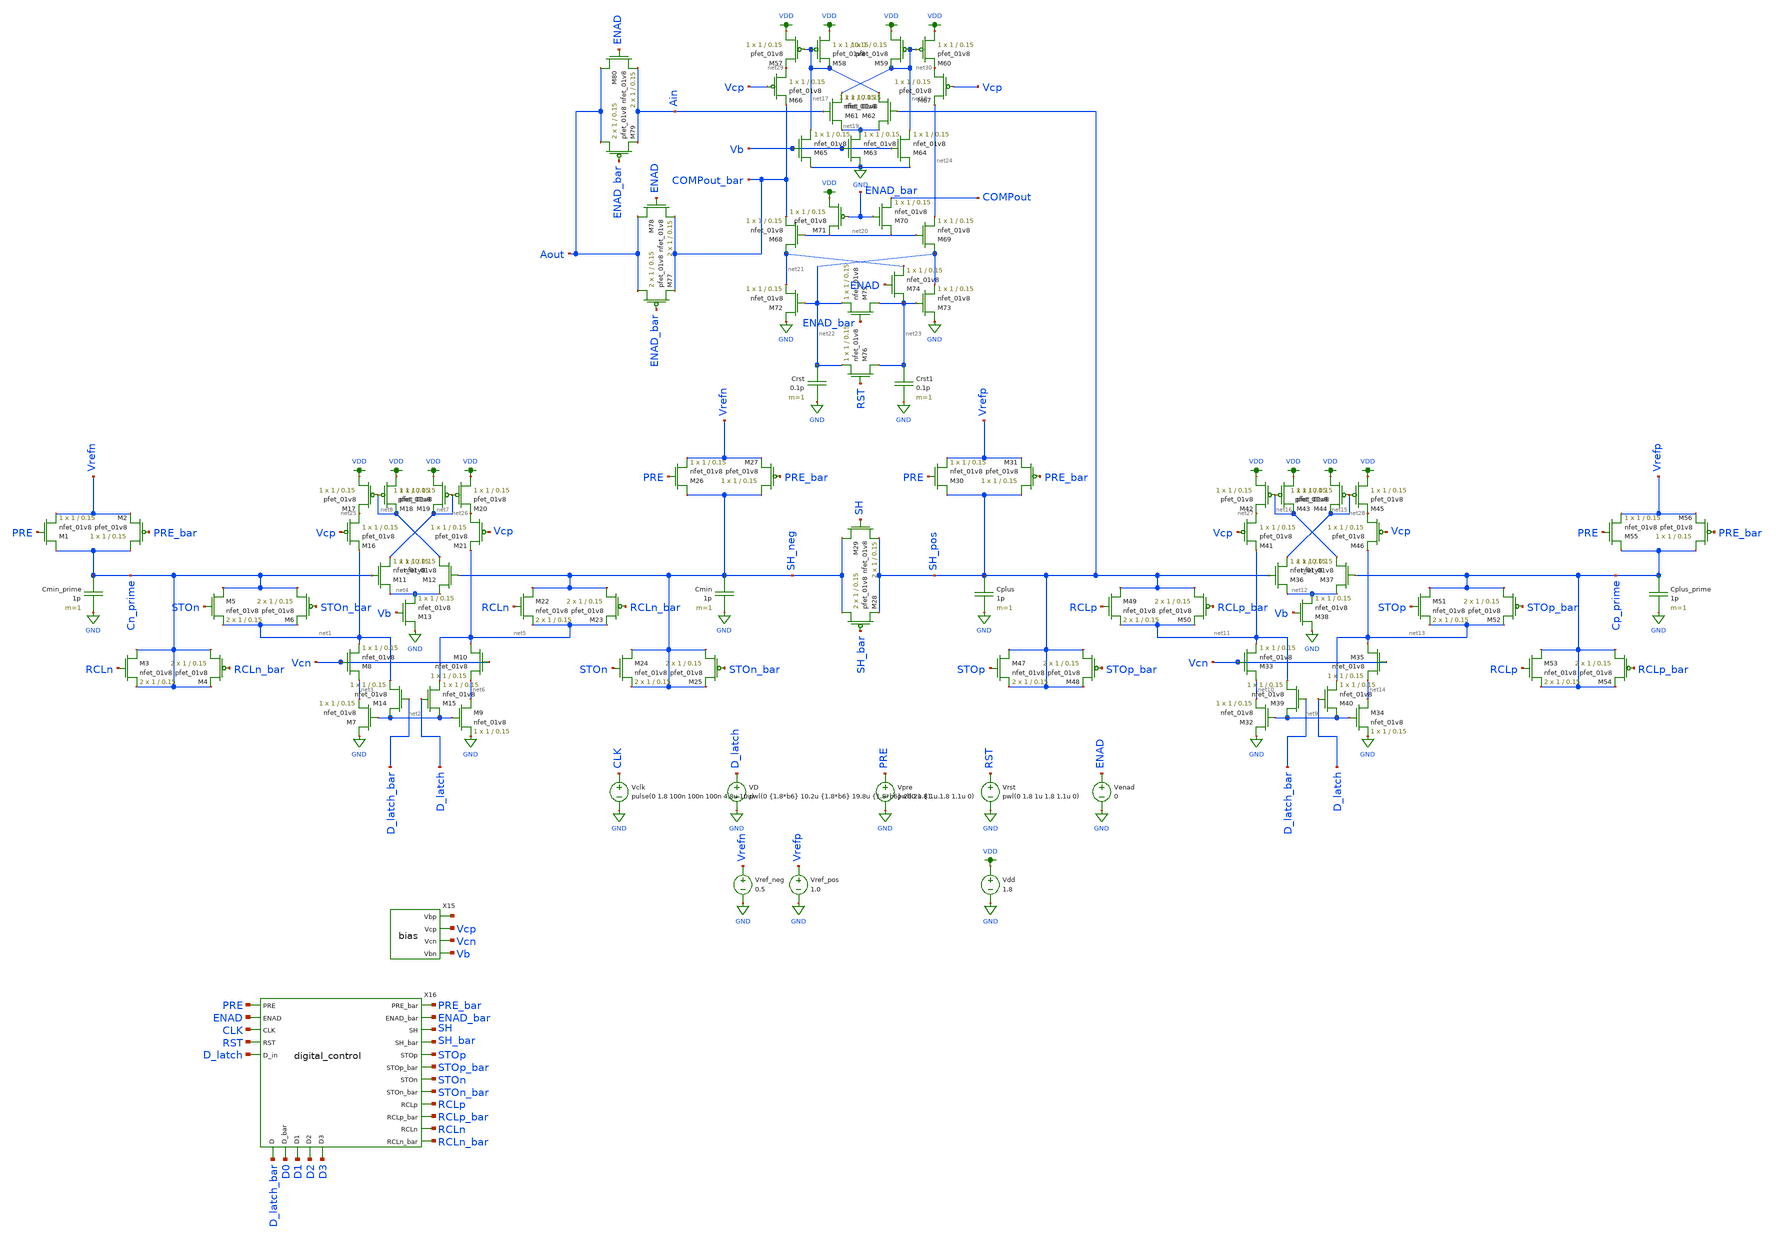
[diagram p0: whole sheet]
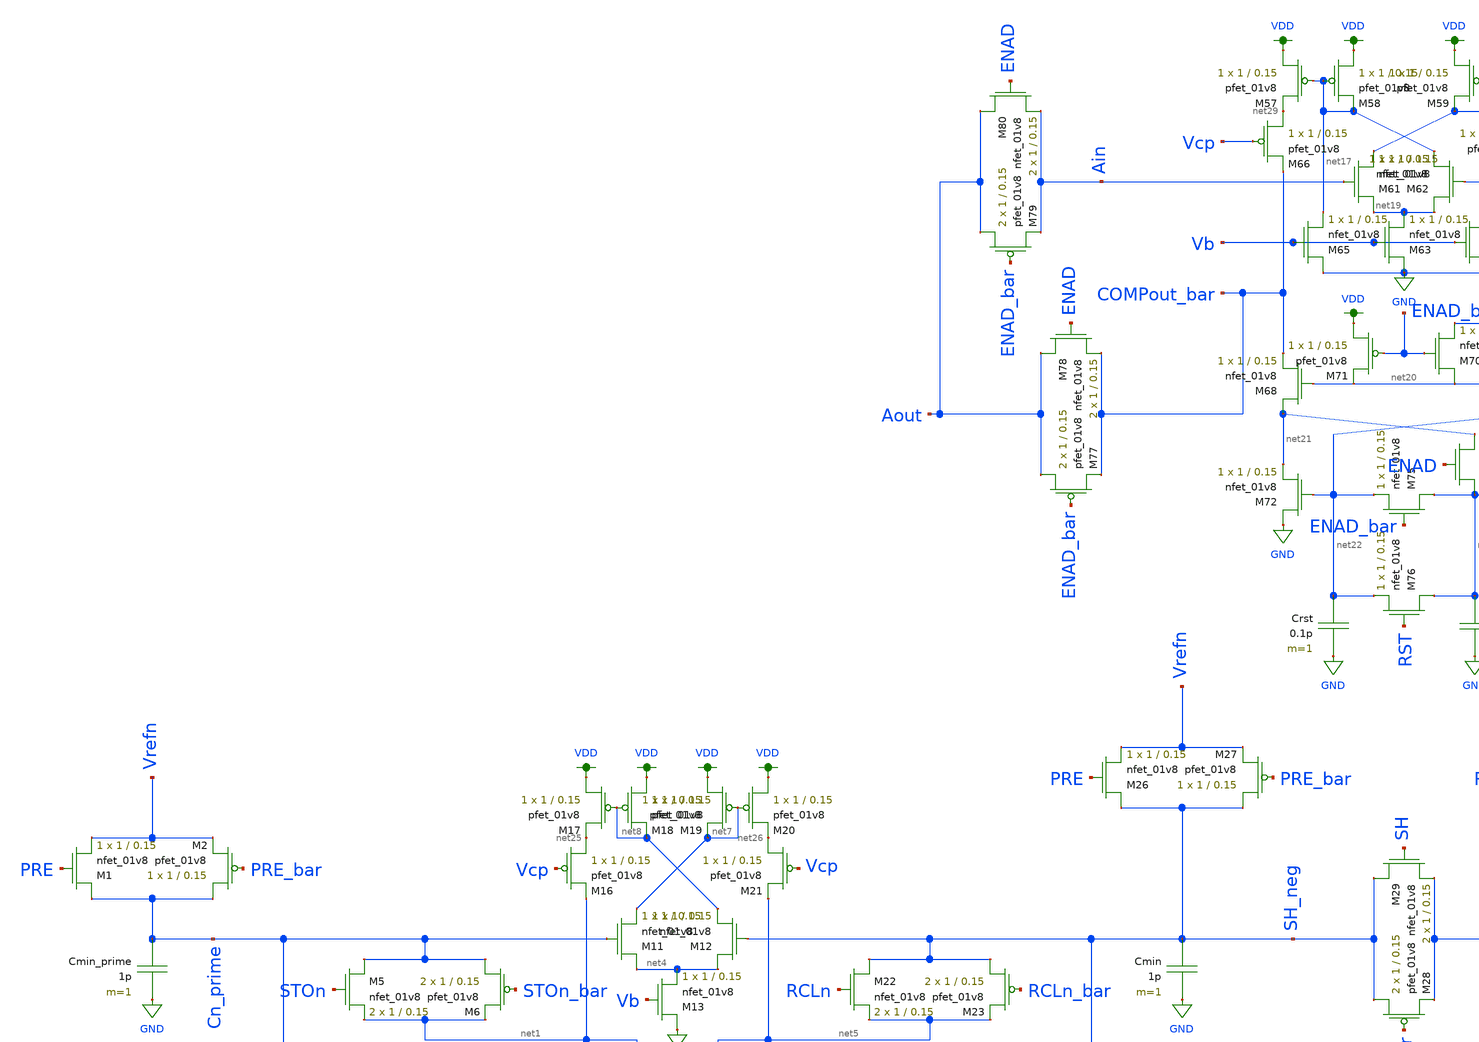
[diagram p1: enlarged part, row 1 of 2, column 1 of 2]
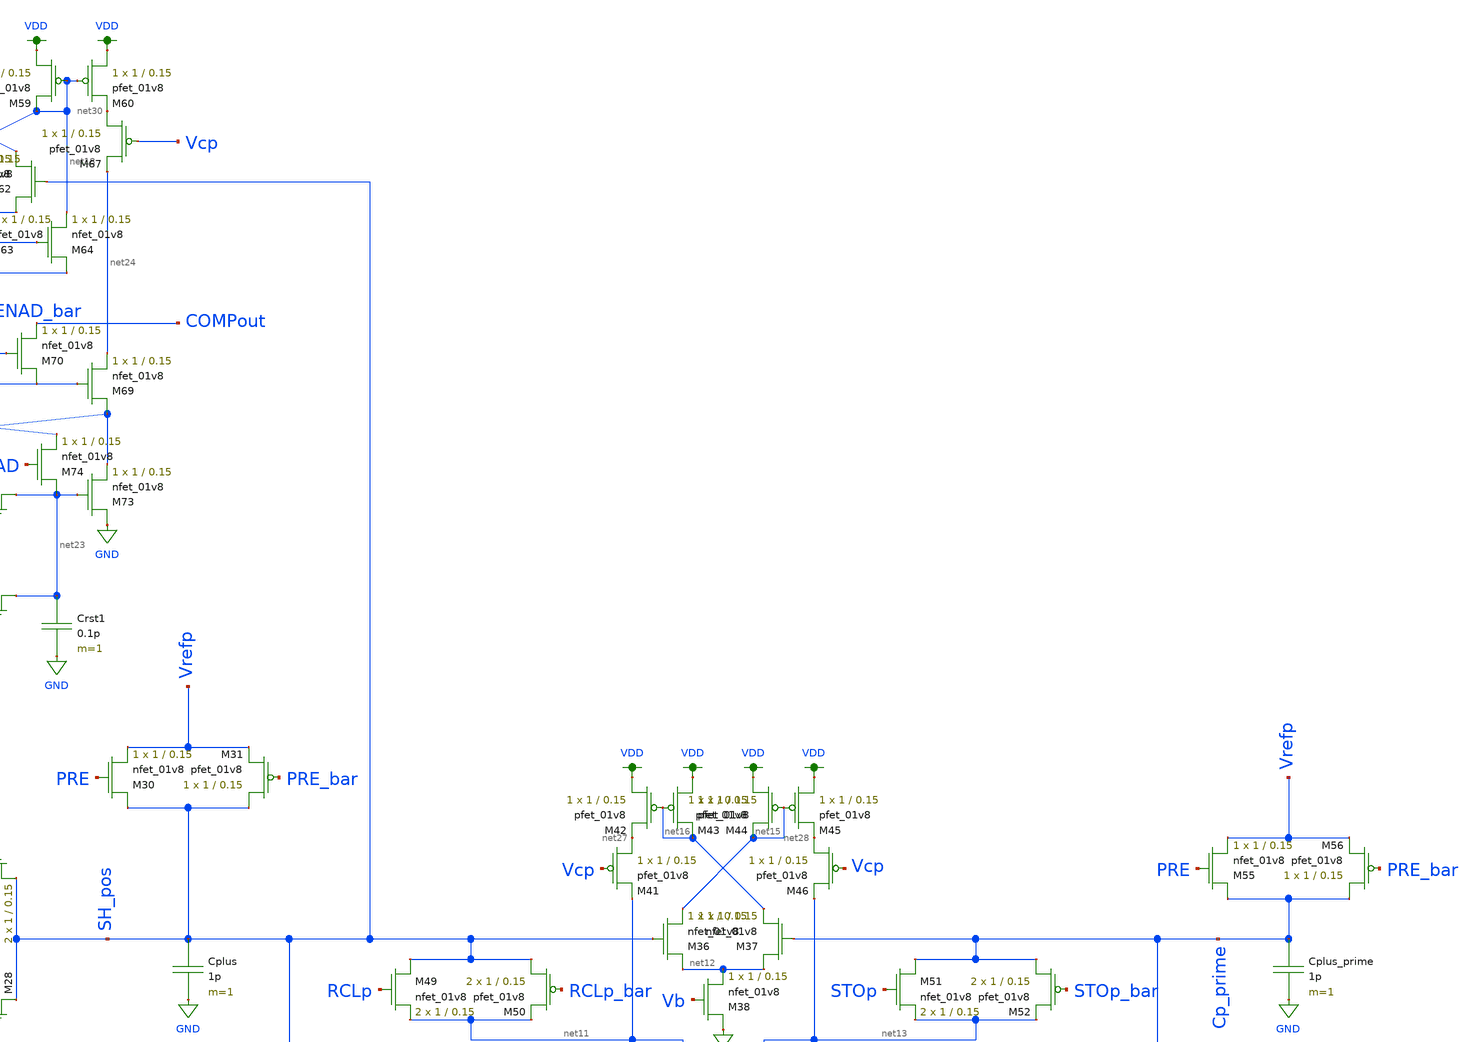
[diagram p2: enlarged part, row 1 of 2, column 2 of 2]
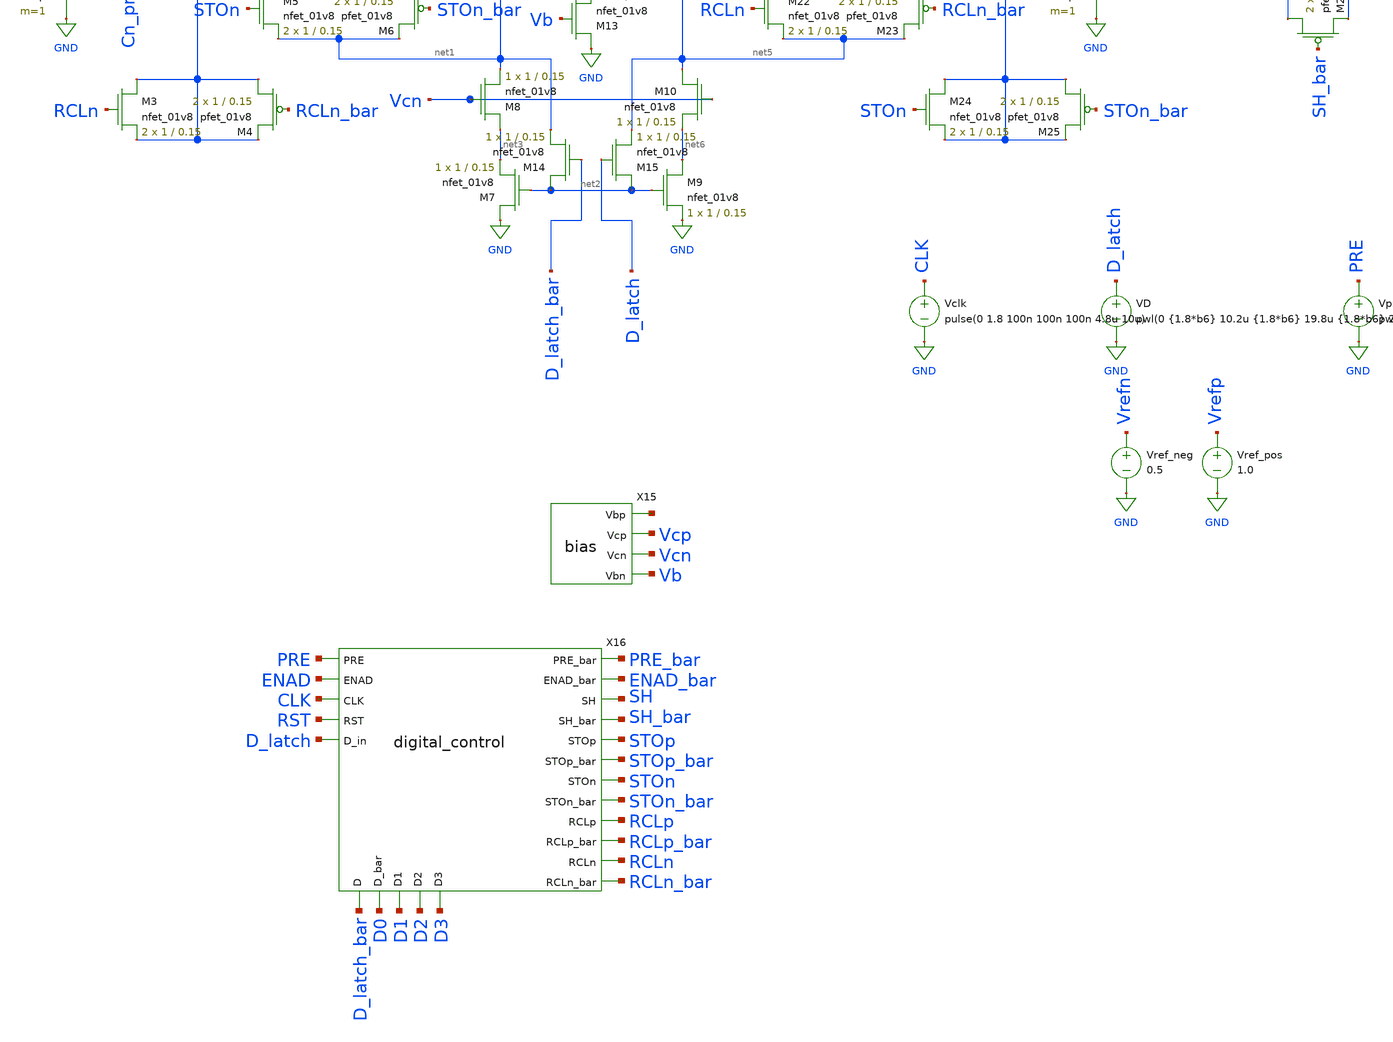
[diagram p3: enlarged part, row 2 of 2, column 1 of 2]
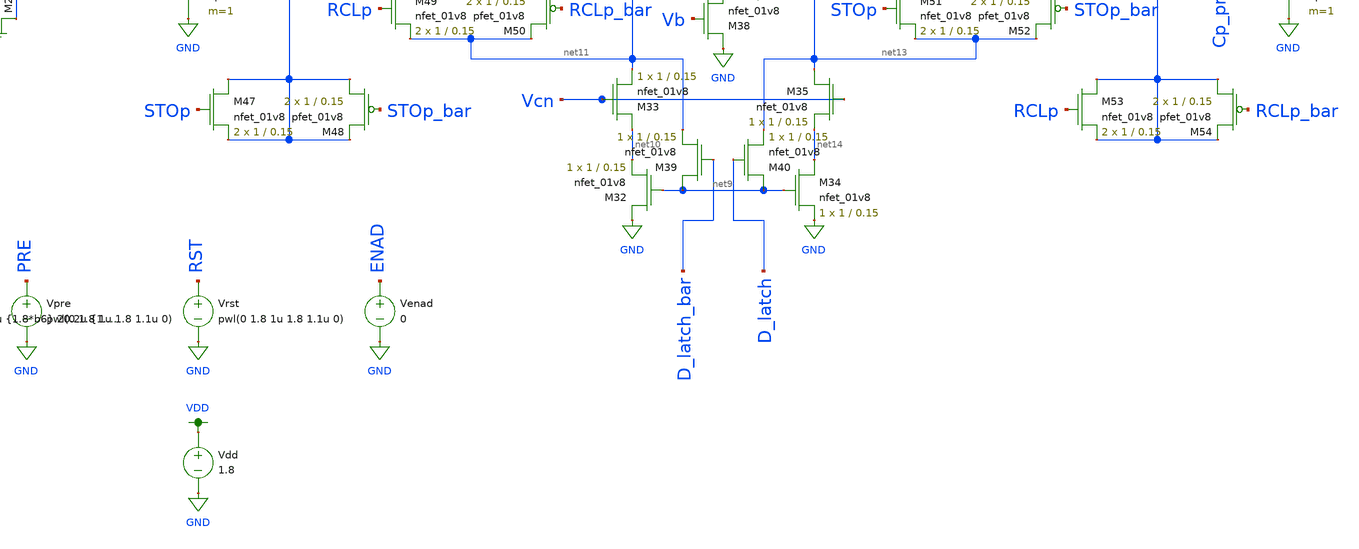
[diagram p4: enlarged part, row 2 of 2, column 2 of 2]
** sch_path: simulations/test_harness_dac_7bit.sch
**.subckt test_harness_dac_7bit
XM1 Cn_prime PRE Vrefn GND sky130_fd_pr__nfet_01v8 L=0.15 W=1 nf=1 ad='int((nf+1)/2) * W/nf * 0.29' as='int((nf+2)/2) * W/nf * 0.29'
+ pd='2*int((nf+1)/2) * (W/nf + 0.29)' ps='2*int((nf+2)/2) * (W/nf + 0.29)' nrd='0.29 / W' nrs='0.29 / W'
+ sa=0 sb=0 sd=0 mult=1 m=1
XM2 Cn_prime PRE_bar Vrefn VDD sky130_fd_pr__pfet_01v8 L=0.15 W=1 nf=1 ad='int((nf+1)/2) * W/nf * 0.29'
+ as='int((nf+2)/2) * W/nf * 0.29' pd='2*int((nf+1)/2) * (W/nf + 0.29)' ps='2*int((nf+2)/2) * (W/nf + 0.29)'
+ nrd='0.29 / W' nrs='0.29 / W' sa=0 sb=0 sd=0 mult=1 m=1
Cmin_prime Cn_prime GND 1p m=1
XM3 Cn_prime RCLn Cn_prime GND sky130_fd_pr__nfet_01v8 L=0.15 W=1 nf=1 ad='int((nf+1)/2) * W/nf * 0.29'
+ as='int((nf+2)/2) * W/nf * 0.29' pd='2*int((nf+1)/2) * (W/nf + 0.29)' ps='2*int((nf+2)/2) * (W/nf + 0.29)'
+ nrd='0.29 / W' nrs='0.29 / W' sa=0 sb=0 sd=0 mult=2 m=2
XM4 Cn_prime RCLn_bar Cn_prime VDD sky130_fd_pr__pfet_01v8 L=0.15 W=1 nf=1 ad='int((nf+1)/2) * W/nf * 0.29'
+ as='int((nf+2)/2) * W/nf * 0.29' pd='2*int((nf+1)/2) * (W/nf + 0.29)' ps='2*int((nf+2)/2) * (W/nf + 0.29)'
+ nrd='0.29 / W' nrs='0.29 / W' sa=0 sb=0 sd=0 mult=2 m=2
XM5 Cn_prime STOn net1 GND sky130_fd_pr__nfet_01v8 L=0.15 W=1 nf=1 ad='int((nf+1)/2) * W/nf * 0.29' as='int((nf+2)/2) * W/nf * 0.29'
+ pd='2*int((nf+1)/2) * (W/nf + 0.29)' ps='2*int((nf+2)/2) * (W/nf + 0.29)' nrd='0.29 / W' nrs='0.29 / W'
+ sa=0 sb=0 sd=0 mult=2 m=2
XM6 Cn_prime STOn_bar net1 VDD sky130_fd_pr__pfet_01v8 L=0.15 W=1 nf=1 ad='int((nf+1)/2) * W/nf * 0.29'
+ as='int((nf+2)/2) * W/nf * 0.29' pd='2*int((nf+1)/2) * (W/nf + 0.29)' ps='2*int((nf+2)/2) * (W/nf + 0.29)'
+ nrd='0.29 / W' nrs='0.29 / W' sa=0 sb=0 sd=0 mult=2 m=2
XM7 GND net2 net3 GND sky130_fd_pr__nfet_01v8 L=0.15 W=1 nf=1 ad='int((nf+1)/2) * W/nf * 0.29' as='int((nf+2)/2) * W/nf * 0.29'
+ pd='2*int((nf+1)/2) * (W/nf + 0.29)' ps='2*int((nf+2)/2) * (W/nf + 0.29)' nrd='0.29 / W' nrs='0.29 / W'
+ sa=0 sb=0 sd=0 mult=1 m=1
XM8 net3 Vcn net1 GND sky130_fd_pr__nfet_01v8 L=0.15 W=1 nf=1 ad='int((nf+1)/2) * W/nf * 0.29' as='int((nf+2)/2) * W/nf * 0.29'
+ pd='2*int((nf+1)/2) * (W/nf + 0.29)' ps='2*int((nf+2)/2) * (W/nf + 0.29)' nrd='0.29 / W' nrs='0.29 / W'
+ sa=0 sb=0 sd=0 mult=1 m=1
XM9 net6 net2 GND GND sky130_fd_pr__nfet_01v8 L=0.15 W=1 nf=1 ad='int((nf+1)/2) * W/nf * 0.29' as='int((nf+2)/2) * W/nf * 0.29'
+ pd='2*int((nf+1)/2) * (W/nf + 0.29)' ps='2*int((nf+2)/2) * (W/nf + 0.29)' nrd='0.29 / W' nrs='0.29 / W'
+ sa=0 sb=0 sd=0 mult=1 m=1
XM10 net5 Vcn net6 GND sky130_fd_pr__nfet_01v8 L=0.15 W=1 nf=1 ad='int((nf+1)/2) * W/nf * 0.29' as='int((nf+2)/2) * W/nf * 0.29'
+ pd='2*int((nf+1)/2) * (W/nf + 0.29)' ps='2*int((nf+2)/2) * (W/nf + 0.29)' nrd='0.29 / W' nrs='0.29 / W'
+ sa=0 sb=0 sd=0 mult=1 m=1
XM11 net4 Cn_prime net7 GND sky130_fd_pr__nfet_01v8 L=0.15 W=1 nf=1 ad='int((nf+1)/2) * W/nf * 0.29'
+ as='int((nf+2)/2) * W/nf * 0.29' pd='2*int((nf+1)/2) * (W/nf + 0.29)' ps='2*int((nf+2)/2) * (W/nf + 0.29)'
+ nrd='0.29 / W' nrs='0.29 / W' sa=0 sb=0 sd=0 mult=1 m=1
XM12 net4 SH_neg net8 GND sky130_fd_pr__nfet_01v8 L=0.15 W=1 nf=1 ad='int((nf+1)/2) * W/nf * 0.29' as='int((nf+2)/2) * W/nf * 0.29'
+ pd='2*int((nf+1)/2) * (W/nf + 0.29)' ps='2*int((nf+2)/2) * (W/nf + 0.29)' nrd='0.29 / W' nrs='0.29 / W'
+ sa=0 sb=0 sd=0 mult=1 m=1
XM13 GND Vb net4 GND sky130_fd_pr__nfet_01v8 L=0.15 W=1 nf=1 ad='int((nf+1)/2) * W/nf * 0.29' as='int((nf+2)/2) * W/nf * 0.29'
+ pd='2*int((nf+1)/2) * (W/nf + 0.29)' ps='2*int((nf+2)/2) * (W/nf + 0.29)' nrd='0.29 / W' nrs='0.29 / W'
+ sa=0 sb=0 sd=0 mult=1 m=1
XM14 net2 D_latch_bar net1 GND sky130_fd_pr__nfet_01v8 L=0.15 W=1 nf=1 ad='int((nf+1)/2) * W/nf * 0.29'
+ as='int((nf+2)/2) * W/nf * 0.29' pd='2*int((nf+1)/2) * (W/nf + 0.29)' ps='2*int((nf+2)/2) * (W/nf + 0.29)'
+ nrd='0.29 / W' nrs='0.29 / W' sa=0 sb=0 sd=0 mult=1 m=1
XM15 net2 D_latch net5 GND sky130_fd_pr__nfet_01v8 L=0.15 W=1 nf=1 ad='int((nf+1)/2) * W/nf * 0.29' as='int((nf+2)/2) * W/nf * 0.29'
+ pd='2*int((nf+1)/2) * (W/nf + 0.29)' ps='2*int((nf+2)/2) * (W/nf + 0.29)' nrd='0.29 / W' nrs='0.29 / W'
+ sa=0 sb=0 sd=0 mult=1 m=1
XM16 net25 Vcp net1 VDD sky130_fd_pr__pfet_01v8 L=0.15 W=1 nf=1 ad='int((nf+1)/2) * W/nf * 0.29' as='int((nf+2)/2) * W/nf * 0.29'
+ pd='2*int((nf+1)/2) * (W/nf + 0.29)' ps='2*int((nf+2)/2) * (W/nf + 0.29)' nrd='0.29 / W' nrs='0.29 / W'
+ sa=0 sb=0 sd=0 mult=1 m=1
XM17 VDD net8 net25 VDD sky130_fd_pr__pfet_01v8 L=0.15 W=1 nf=1 ad='int((nf+1)/2) * W/nf * 0.29' as='int((nf+2)/2) * W/nf * 0.29'
+ pd='2*int((nf+1)/2) * (W/nf + 0.29)' ps='2*int((nf+2)/2) * (W/nf + 0.29)' nrd='0.29 / W' nrs='0.29 / W'
+ sa=0 sb=0 sd=0 mult=1 m=1
XM18 VDD net8 net8 VDD sky130_fd_pr__pfet_01v8 L=0.15 W=1 nf=1 ad='int((nf+1)/2) * W/nf * 0.29' as='int((nf+2)/2) * W/nf * 0.29'
+ pd='2*int((nf+1)/2) * (W/nf + 0.29)' ps='2*int((nf+2)/2) * (W/nf + 0.29)' nrd='0.29 / W' nrs='0.29 / W'
+ sa=0 sb=0 sd=0 mult=1 m=1
XM19 VDD net7 net7 VDD sky130_fd_pr__pfet_01v8 L=0.15 W=1 nf=1 ad='int((nf+1)/2) * W/nf * 0.29' as='int((nf+2)/2) * W/nf * 0.29'
+ pd='2*int((nf+1)/2) * (W/nf + 0.29)' ps='2*int((nf+2)/2) * (W/nf + 0.29)' nrd='0.29 / W' nrs='0.29 / W'
+ sa=0 sb=0 sd=0 mult=1 m=1
XM20 VDD net7 net26 VDD sky130_fd_pr__pfet_01v8 L=0.15 W=1 nf=1 ad='int((nf+1)/2) * W/nf * 0.29' as='int((nf+2)/2) * W/nf * 0.29'
+ pd='2*int((nf+1)/2) * (W/nf + 0.29)' ps='2*int((nf+2)/2) * (W/nf + 0.29)' nrd='0.29 / W' nrs='0.29 / W'
+ sa=0 sb=0 sd=0 mult=1 m=1
XM21 net26 Vcp net5 VDD sky130_fd_pr__pfet_01v8 L=0.15 W=1 nf=1 ad='int((nf+1)/2) * W/nf * 0.29' as='int((nf+2)/2) * W/nf * 0.29'
+ pd='2*int((nf+1)/2) * (W/nf + 0.29)' ps='2*int((nf+2)/2) * (W/nf + 0.29)' nrd='0.29 / W' nrs='0.29 / W'
+ sa=0 sb=0 sd=0 mult=1 m=1
XM22 SH_neg RCLn net5 GND sky130_fd_pr__nfet_01v8 L=0.15 W=1 nf=1 ad='int((nf+1)/2) * W/nf * 0.29' as='int((nf+2)/2) * W/nf * 0.29'
+ pd='2*int((nf+1)/2) * (W/nf + 0.29)' ps='2*int((nf+2)/2) * (W/nf + 0.29)' nrd='0.29 / W' nrs='0.29 / W'
+ sa=0 sb=0 sd=0 mult=2 m=2
XM23 SH_neg RCLn_bar net5 VDD sky130_fd_pr__pfet_01v8 L=0.15 W=1 nf=1 ad='int((nf+1)/2) * W/nf * 0.29'
+ as='int((nf+2)/2) * W/nf * 0.29' pd='2*int((nf+1)/2) * (W/nf + 0.29)' ps='2*int((nf+2)/2) * (W/nf + 0.29)'
+ nrd='0.29 / W' nrs='0.29 / W' sa=0 sb=0 sd=0 mult=2 m=2
XM24 SH_neg STOn SH_neg GND sky130_fd_pr__nfet_01v8 L=0.15 W=1 nf=1 ad='int((nf+1)/2) * W/nf * 0.29'
+ as='int((nf+2)/2) * W/nf * 0.29' pd='2*int((nf+1)/2) * (W/nf + 0.29)' ps='2*int((nf+2)/2) * (W/nf + 0.29)'
+ nrd='0.29 / W' nrs='0.29 / W' sa=0 sb=0 sd=0 mult=2 m=2
XM25 SH_neg STOn_bar SH_neg VDD sky130_fd_pr__pfet_01v8 L=0.15 W=1 nf=1 ad='int((nf+1)/2) * W/nf * 0.29'
+ as='int((nf+2)/2) * W/nf * 0.29' pd='2*int((nf+1)/2) * (W/nf + 0.29)' ps='2*int((nf+2)/2) * (W/nf + 0.29)'
+ nrd='0.29 / W' nrs='0.29 / W' sa=0 sb=0 sd=0 mult=2 m=2
XM26 SH_neg PRE Vrefn GND sky130_fd_pr__nfet_01v8 L=0.15 W=1 nf=1 ad='int((nf+1)/2) * W/nf * 0.29' as='int((nf+2)/2) * W/nf * 0.29'
+ pd='2*int((nf+1)/2) * (W/nf + 0.29)' ps='2*int((nf+2)/2) * (W/nf + 0.29)' nrd='0.29 / W' nrs='0.29 / W'
+ sa=0 sb=0 sd=0 mult=1 m=1
XM27 SH_neg PRE_bar Vrefn VDD sky130_fd_pr__pfet_01v8 L=0.15 W=1 nf=1 ad='int((nf+1)/2) * W/nf * 0.29'
+ as='int((nf+2)/2) * W/nf * 0.29' pd='2*int((nf+1)/2) * (W/nf + 0.29)' ps='2*int((nf+2)/2) * (W/nf + 0.29)'
+ nrd='0.29 / W' nrs='0.29 / W' sa=0 sb=0 sd=0 mult=1 m=1
Cmin SH_neg GND 1p m=1
XM28 SH_neg SH_bar SH_pos VDD sky130_fd_pr__pfet_01v8 L=0.15 W=1 nf=1 ad='int((nf+1)/2) * W/nf * 0.29'
+ as='int((nf+2)/2) * W/nf * 0.29' pd='2*int((nf+1)/2) * (W/nf + 0.29)' ps='2*int((nf+2)/2) * (W/nf + 0.29)'
+ nrd='0.29 / W' nrs='0.29 / W' sa=0 sb=0 sd=0 mult=2 m=2
XM29 SH_neg SH SH_pos GND sky130_fd_pr__nfet_01v8 L=0.15 W=1 nf=1 ad='int((nf+1)/2) * W/nf * 0.29' as='int((nf+2)/2) * W/nf * 0.29'
+ pd='2*int((nf+1)/2) * (W/nf + 0.29)' ps='2*int((nf+2)/2) * (W/nf + 0.29)' nrd='0.29 / W' nrs='0.29 / W'
+ sa=0 sb=0 sd=0 mult=2 m=2
XM30 SH_pos PRE Vrefp GND sky130_fd_pr__nfet_01v8 L=0.15 W=1 nf=1 ad='int((nf+1)/2) * W/nf * 0.29' as='int((nf+2)/2) * W/nf * 0.29'
+ pd='2*int((nf+1)/2) * (W/nf + 0.29)' ps='2*int((nf+2)/2) * (W/nf + 0.29)' nrd='0.29 / W' nrs='0.29 / W'
+ sa=0 sb=0 sd=0 mult=1 m=1
XM31 SH_pos PRE_bar Vrefp VDD sky130_fd_pr__pfet_01v8 L=0.15 W=1 nf=1 ad='int((nf+1)/2) * W/nf * 0.29'
+ as='int((nf+2)/2) * W/nf * 0.29' pd='2*int((nf+1)/2) * (W/nf + 0.29)' ps='2*int((nf+2)/2) * (W/nf + 0.29)'
+ nrd='0.29 / W' nrs='0.29 / W' sa=0 sb=0 sd=0 mult=1 m=1
Cplus SH_pos GND 1p m=1
XM32 GND net9 net10 GND sky130_fd_pr__nfet_01v8 L=0.15 W=1 nf=1 ad='int((nf+1)/2) * W/nf * 0.29' as='int((nf+2)/2) * W/nf * 0.29'
+ pd='2*int((nf+1)/2) * (W/nf + 0.29)' ps='2*int((nf+2)/2) * (W/nf + 0.29)' nrd='0.29 / W' nrs='0.29 / W'
+ sa=0 sb=0 sd=0 mult=1 m=1
XM33 net10 Vcn net11 GND sky130_fd_pr__nfet_01v8 L=0.15 W=1 nf=1 ad='int((nf+1)/2) * W/nf * 0.29' as='int((nf+2)/2) * W/nf * 0.29'
+ pd='2*int((nf+1)/2) * (W/nf + 0.29)' ps='2*int((nf+2)/2) * (W/nf + 0.29)' nrd='0.29 / W' nrs='0.29 / W'
+ sa=0 sb=0 sd=0 mult=1 m=1
XM34 net14 net9 GND GND sky130_fd_pr__nfet_01v8 L=0.15 W=1 nf=1 ad='int((nf+1)/2) * W/nf * 0.29' as='int((nf+2)/2) * W/nf * 0.29'
+ pd='2*int((nf+1)/2) * (W/nf + 0.29)' ps='2*int((nf+2)/2) * (W/nf + 0.29)' nrd='0.29 / W' nrs='0.29 / W'
+ sa=0 sb=0 sd=0 mult=1 m=1
XM35 net13 Vcn net14 GND sky130_fd_pr__nfet_01v8 L=0.15 W=1 nf=1 ad='int((nf+1)/2) * W/nf * 0.29' as='int((nf+2)/2) * W/nf * 0.29'
+ pd='2*int((nf+1)/2) * (W/nf + 0.29)' ps='2*int((nf+2)/2) * (W/nf + 0.29)' nrd='0.29 / W' nrs='0.29 / W'
+ sa=0 sb=0 sd=0 mult=1 m=1
XM36 net12 SH_pos net15 GND sky130_fd_pr__nfet_01v8 L=0.15 W=1 nf=1 ad='int((nf+1)/2) * W/nf * 0.29'
+ as='int((nf+2)/2) * W/nf * 0.29' pd='2*int((nf+1)/2) * (W/nf + 0.29)' ps='2*int((nf+2)/2) * (W/nf + 0.29)'
+ nrd='0.29 / W' nrs='0.29 / W' sa=0 sb=0 sd=0 mult=1 m=1
XM37 net12 Cp_prime net16 GND sky130_fd_pr__nfet_01v8 L=0.15 W=1 nf=1 ad='int((nf+1)/2) * W/nf * 0.29'
+ as='int((nf+2)/2) * W/nf * 0.29' pd='2*int((nf+1)/2) * (W/nf + 0.29)' ps='2*int((nf+2)/2) * (W/nf + 0.29)'
+ nrd='0.29 / W' nrs='0.29 / W' sa=0 sb=0 sd=0 mult=1 m=1
XM38 GND Vb net12 GND sky130_fd_pr__nfet_01v8 L=0.15 W=1 nf=1 ad='int((nf+1)/2) * W/nf * 0.29' as='int((nf+2)/2) * W/nf * 0.29'
+ pd='2*int((nf+1)/2) * (W/nf + 0.29)' ps='2*int((nf+2)/2) * (W/nf + 0.29)' nrd='0.29 / W' nrs='0.29 / W'
+ sa=0 sb=0 sd=0 mult=1 m=1
XM39 net9 D_latch_bar net11 GND sky130_fd_pr__nfet_01v8 L=0.15 W=1 nf=1 ad='int((nf+1)/2) * W/nf * 0.29'
+ as='int((nf+2)/2) * W/nf * 0.29' pd='2*int((nf+1)/2) * (W/nf + 0.29)' ps='2*int((nf+2)/2) * (W/nf + 0.29)'
+ nrd='0.29 / W' nrs='0.29 / W' sa=0 sb=0 sd=0 mult=1 m=1
XM40 net9 D_latch net13 GND sky130_fd_pr__nfet_01v8 L=0.15 W=1 nf=1 ad='int((nf+1)/2) * W/nf * 0.29'
+ as='int((nf+2)/2) * W/nf * 0.29' pd='2*int((nf+1)/2) * (W/nf + 0.29)' ps='2*int((nf+2)/2) * (W/nf + 0.29)'
+ nrd='0.29 / W' nrs='0.29 / W' sa=0 sb=0 sd=0 mult=1 m=1
XM41 net27 Vcp net11 VDD sky130_fd_pr__pfet_01v8 L=0.15 W=1 nf=1 ad='int((nf+1)/2) * W/nf * 0.29' as='int((nf+2)/2) * W/nf * 0.29'
+ pd='2*int((nf+1)/2) * (W/nf + 0.29)' ps='2*int((nf+2)/2) * (W/nf + 0.29)' nrd='0.29 / W' nrs='0.29 / W'
+ sa=0 sb=0 sd=0 mult=1 m=1
XM42 VDD net16 net27 VDD sky130_fd_pr__pfet_01v8 L=0.15 W=1 nf=1 ad='int((nf+1)/2) * W/nf * 0.29' as='int((nf+2)/2) * W/nf * 0.29'
+ pd='2*int((nf+1)/2) * (W/nf + 0.29)' ps='2*int((nf+2)/2) * (W/nf + 0.29)' nrd='0.29 / W' nrs='0.29 / W'
+ sa=0 sb=0 sd=0 mult=1 m=1
XM43 VDD net16 net16 VDD sky130_fd_pr__pfet_01v8 L=0.15 W=1 nf=1 ad='int((nf+1)/2) * W/nf * 0.29' as='int((nf+2)/2) * W/nf * 0.29'
+ pd='2*int((nf+1)/2) * (W/nf + 0.29)' ps='2*int((nf+2)/2) * (W/nf + 0.29)' nrd='0.29 / W' nrs='0.29 / W'
+ sa=0 sb=0 sd=0 mult=1 m=1
XM44 VDD net15 net15 VDD sky130_fd_pr__pfet_01v8 L=0.15 W=1 nf=1 ad='int((nf+1)/2) * W/nf * 0.29' as='int((nf+2)/2) * W/nf * 0.29'
+ pd='2*int((nf+1)/2) * (W/nf + 0.29)' ps='2*int((nf+2)/2) * (W/nf + 0.29)' nrd='0.29 / W' nrs='0.29 / W'
+ sa=0 sb=0 sd=0 mult=1 m=1
XM45 VDD net15 net28 VDD sky130_fd_pr__pfet_01v8 L=0.15 W=1 nf=1 ad='int((nf+1)/2) * W/nf * 0.29' as='int((nf+2)/2) * W/nf * 0.29'
+ pd='2*int((nf+1)/2) * (W/nf + 0.29)' ps='2*int((nf+2)/2) * (W/nf + 0.29)' nrd='0.29 / W' nrs='0.29 / W'
+ sa=0 sb=0 sd=0 mult=1 m=1
XM46 net28 Vcp net13 VDD sky130_fd_pr__pfet_01v8 L=0.15 W=1 nf=1 ad='int((nf+1)/2) * W/nf * 0.29' as='int((nf+2)/2) * W/nf * 0.29'
+ pd='2*int((nf+1)/2) * (W/nf + 0.29)' ps='2*int((nf+2)/2) * (W/nf + 0.29)' nrd='0.29 / W' nrs='0.29 / W'
+ sa=0 sb=0 sd=0 mult=1 m=1
XM47 SH_pos STOp SH_pos GND sky130_fd_pr__nfet_01v8 L=0.15 W=1 nf=1 ad='int((nf+1)/2) * W/nf * 0.29'
+ as='int((nf+2)/2) * W/nf * 0.29' pd='2*int((nf+1)/2) * (W/nf + 0.29)' ps='2*int((nf+2)/2) * (W/nf + 0.29)'
+ nrd='0.29 / W' nrs='0.29 / W' sa=0 sb=0 sd=0 mult=2 m=2
XM48 SH_pos STOp_bar SH_pos VDD sky130_fd_pr__pfet_01v8 L=0.15 W=1 nf=1 ad='int((nf+1)/2) * W/nf * 0.29'
+ as='int((nf+2)/2) * W/nf * 0.29' pd='2*int((nf+1)/2) * (W/nf + 0.29)' ps='2*int((nf+2)/2) * (W/nf + 0.29)'
+ nrd='0.29 / W' nrs='0.29 / W' sa=0 sb=0 sd=0 mult=2 m=2
XM49 SH_pos RCLp net11 GND sky130_fd_pr__nfet_01v8 L=0.15 W=1 nf=1 ad='int((nf+1)/2) * W/nf * 0.29' as='int((nf+2)/2) * W/nf * 0.29'
+ pd='2*int((nf+1)/2) * (W/nf + 0.29)' ps='2*int((nf+2)/2) * (W/nf + 0.29)' nrd='0.29 / W' nrs='0.29 / W'
+ sa=0 sb=0 sd=0 mult=2 m=2
XM50 SH_pos RCLp_bar net11 VDD sky130_fd_pr__pfet_01v8 L=0.15 W=1 nf=1 ad='int((nf+1)/2) * W/nf * 0.29'
+ as='int((nf+2)/2) * W/nf * 0.29' pd='2*int((nf+1)/2) * (W/nf + 0.29)' ps='2*int((nf+2)/2) * (W/nf + 0.29)'
+ nrd='0.29 / W' nrs='0.29 / W' sa=0 sb=0 sd=0 mult=2 m=2
XM51 Cp_prime STOp net13 GND sky130_fd_pr__nfet_01v8 L=0.15 W=1 nf=1 ad='int((nf+1)/2) * W/nf * 0.29'
+ as='int((nf+2)/2) * W/nf * 0.29' pd='2*int((nf+1)/2) * (W/nf + 0.29)' ps='2*int((nf+2)/2) * (W/nf + 0.29)'
+ nrd='0.29 / W' nrs='0.29 / W' sa=0 sb=0 sd=0 mult=2 m=2
XM52 Cp_prime STOp_bar net13 VDD sky130_fd_pr__pfet_01v8 L=0.15 W=1 nf=1 ad='int((nf+1)/2) * W/nf * 0.29'
+ as='int((nf+2)/2) * W/nf * 0.29' pd='2*int((nf+1)/2) * (W/nf + 0.29)' ps='2*int((nf+2)/2) * (W/nf + 0.29)'
+ nrd='0.29 / W' nrs='0.29 / W' sa=0 sb=0 sd=0 mult=2 m=2
XM53 Cp_prime RCLp Cp_prime GND sky130_fd_pr__nfet_01v8 L=0.15 W=1 nf=1 ad='int((nf+1)/2) * W/nf * 0.29'
+ as='int((nf+2)/2) * W/nf * 0.29' pd='2*int((nf+1)/2) * (W/nf + 0.29)' ps='2*int((nf+2)/2) * (W/nf + 0.29)'
+ nrd='0.29 / W' nrs='0.29 / W' sa=0 sb=0 sd=0 mult=2 m=2
XM54 Cp_prime RCLp_bar Cp_prime VDD sky130_fd_pr__pfet_01v8 L=0.15 W=1 nf=1 ad='int((nf+1)/2) * W/nf * 0.29'
+ as='int((nf+2)/2) * W/nf * 0.29' pd='2*int((nf+1)/2) * (W/nf + 0.29)' ps='2*int((nf+2)/2) * (W/nf + 0.29)'
+ nrd='0.29 / W' nrs='0.29 / W' sa=0 sb=0 sd=0 mult=2 m=2
XM55 Cp_prime PRE Vrefp GND sky130_fd_pr__nfet_01v8 L=0.15 W=1 nf=1 ad='int((nf+1)/2) * W/nf * 0.29'
+ as='int((nf+2)/2) * W/nf * 0.29' pd='2*int((nf+1)/2) * (W/nf + 0.29)' ps='2*int((nf+2)/2) * (W/nf + 0.29)'
+ nrd='0.29 / W' nrs='0.29 / W' sa=0 sb=0 sd=0 mult=1 m=1
XM56 Cp_prime PRE_bar Vrefp VDD sky130_fd_pr__pfet_01v8 L=0.15 W=1 nf=1 ad='int((nf+1)/2) * W/nf * 0.29'
+ as='int((nf+2)/2) * W/nf * 0.29' pd='2*int((nf+1)/2) * (W/nf + 0.29)' ps='2*int((nf+2)/2) * (W/nf + 0.29)'
+ nrd='0.29 / W' nrs='0.29 / W' sa=0 sb=0 sd=0 mult=1 m=1
Cplus_prime Cp_prime GND 1p m=1
XM57 VDD net17 net29 VDD sky130_fd_pr__pfet_01v8 L=0.15 W=1 nf=1 ad='int((nf+1)/2) * W/nf * 0.29' as='int((nf+2)/2) * W/nf * 0.29'
+ pd='2*int((nf+1)/2) * (W/nf + 0.29)' ps='2*int((nf+2)/2) * (W/nf + 0.29)' nrd='0.29 / W' nrs='0.29 / W'
+ sa=0 sb=0 sd=0 mult=1 m=1
XM58 VDD net17 net17 VDD sky130_fd_pr__pfet_01v8 L=0.15 W=1 nf=1 ad='int((nf+1)/2) * W/nf * 0.29' as='int((nf+2)/2) * W/nf * 0.29'
+ pd='2*int((nf+1)/2) * (W/nf + 0.29)' ps='2*int((nf+2)/2) * (W/nf + 0.29)' nrd='0.29 / W' nrs='0.29 / W'
+ sa=0 sb=0 sd=0 mult=1 m=1
XM59 VDD net18 net18 VDD sky130_fd_pr__pfet_01v8 L=0.15 W=1 nf=1 ad='int((nf+1)/2) * W/nf * 0.29' as='int((nf+2)/2) * W/nf * 0.29'
+ pd='2*int((nf+1)/2) * (W/nf + 0.29)' ps='2*int((nf+2)/2) * (W/nf + 0.29)' nrd='0.29 / W' nrs='0.29 / W'
+ sa=0 sb=0 sd=0 mult=1 m=1
XM60 VDD net18 net30 VDD sky130_fd_pr__pfet_01v8 L=0.15 W=1 nf=1 ad='int((nf+1)/2) * W/nf * 0.29' as='int((nf+2)/2) * W/nf * 0.29'
+ pd='2*int((nf+1)/2) * (W/nf + 0.29)' ps='2*int((nf+2)/2) * (W/nf + 0.29)' nrd='0.29 / W' nrs='0.29 / W'
+ sa=0 sb=0 sd=0 mult=1 m=1
XM61 net19 Ain net18 GND sky130_fd_pr__nfet_01v8 L=0.15 W=1 nf=1 ad='int((nf+1)/2) * W/nf * 0.29' as='int((nf+2)/2) * W/nf * 0.29'
+ pd='2*int((nf+1)/2) * (W/nf + 0.29)' ps='2*int((nf+2)/2) * (W/nf + 0.29)' nrd='0.29 / W' nrs='0.29 / W'
+ sa=0 sb=0 sd=0 mult=1 m=1
XM62 net19 SH_pos net17 GND sky130_fd_pr__nfet_01v8 L=0.15 W=1 nf=1 ad='int((nf+1)/2) * W/nf * 0.29'
+ as='int((nf+2)/2) * W/nf * 0.29' pd='2*int((nf+1)/2) * (W/nf + 0.29)' ps='2*int((nf+2)/2) * (W/nf + 0.29)'
+ nrd='0.29 / W' nrs='0.29 / W' sa=0 sb=0 sd=0 mult=1 m=1
XM63 GND Vb net19 GND sky130_fd_pr__nfet_01v8 L=0.15 W=1 nf=1 ad='int((nf+1)/2) * W/nf * 0.29' as='int((nf+2)/2) * W/nf * 0.29'
+ pd='2*int((nf+1)/2) * (W/nf + 0.29)' ps='2*int((nf+2)/2) * (W/nf + 0.29)' nrd='0.29 / W' nrs='0.29 / W'
+ sa=0 sb=0 sd=0 mult=1 m=1
XM64 GND Vb net18 GND sky130_fd_pr__nfet_01v8 L=0.15 W=1 nf=1 ad='int((nf+1)/2) * W/nf * 0.29' as='int((nf+2)/2) * W/nf * 0.29'
+ pd='2*int((nf+1)/2) * (W/nf + 0.29)' ps='2*int((nf+2)/2) * (W/nf + 0.29)' nrd='0.29 / W' nrs='0.29 / W'
+ sa=0 sb=0 sd=0 mult=1 m=1
XM65 GND Vb net17 GND sky130_fd_pr__nfet_01v8 L=0.15 W=1 nf=1 ad='int((nf+1)/2) * W/nf * 0.29' as='int((nf+2)/2) * W/nf * 0.29'
+ pd='2*int((nf+1)/2) * (W/nf + 0.29)' ps='2*int((nf+2)/2) * (W/nf + 0.29)' nrd='0.29 / W' nrs='0.29 / W'
+ sa=0 sb=0 sd=0 mult=1 m=1
XM66 net29 Vcp COMPout_bar VDD sky130_fd_pr__pfet_01v8 L=0.15 W=1 nf=1 ad='int((nf+1)/2) * W/nf * 0.29'
+ as='int((nf+2)/2) * W/nf * 0.29' pd='2*int((nf+1)/2) * (W/nf + 0.29)' ps='2*int((nf+2)/2) * (W/nf + 0.29)'
+ nrd='0.29 / W' nrs='0.29 / W' sa=0 sb=0 sd=0 mult=1 m=1
XM67 net30 Vcp net24 VDD sky130_fd_pr__pfet_01v8 L=0.15 W=1 nf=1 ad='int((nf+1)/2) * W/nf * 0.29' as='int((nf+2)/2) * W/nf * 0.29'
+ pd='2*int((nf+1)/2) * (W/nf + 0.29)' ps='2*int((nf+2)/2) * (W/nf + 0.29)' nrd='0.29 / W' nrs='0.29 / W'
+ sa=0 sb=0 sd=0 mult=1 m=1
XM68 net21 net20 COMPout_bar GND sky130_fd_pr__nfet_01v8 L=0.15 W=1 nf=1 ad='int((nf+1)/2) * W/nf * 0.29'
+ as='int((nf+2)/2) * W/nf * 0.29' pd='2*int((nf+1)/2) * (W/nf + 0.29)' ps='2*int((nf+2)/2) * (W/nf + 0.29)'
+ nrd='0.29 / W' nrs='0.29 / W' sa=0 sb=0 sd=0 mult=1 m=1
XM69 net22 net20 net24 GND sky130_fd_pr__nfet_01v8 L=0.15 W=1 nf=1 ad='int((nf+1)/2) * W/nf * 0.29' as='int((nf+2)/2) * W/nf * 0.29'
+ pd='2*int((nf+1)/2) * (W/nf + 0.29)' ps='2*int((nf+2)/2) * (W/nf + 0.29)' nrd='0.29 / W' nrs='0.29 / W'
+ sa=0 sb=0 sd=0 mult=1 m=1
XM70 net20 ENAD_bar COMPout GND sky130_fd_pr__nfet_01v8 L=0.15 W=1 nf=1 ad='int((nf+1)/2) * W/nf * 0.29'
+ as='int((nf+2)/2) * W/nf * 0.29' pd='2*int((nf+1)/2) * (W/nf + 0.29)' ps='2*int((nf+2)/2) * (W/nf + 0.29)'
+ nrd='0.29 / W' nrs='0.29 / W' sa=0 sb=0 sd=0 mult=1 m=1
XM71 VDD ENAD_bar net20 VDD sky130_fd_pr__pfet_01v8 L=0.15 W=1 nf=1 ad='int((nf+1)/2) * W/nf * 0.29'
+ as='int((nf+2)/2) * W/nf * 0.29' pd='2*int((nf+1)/2) * (W/nf + 0.29)' ps='2*int((nf+2)/2) * (W/nf + 0.29)'
+ nrd='0.29 / W' nrs='0.29 / W' sa=0 sb=0 sd=0 mult=1 m=1
XM72 GND net22 net21 GND sky130_fd_pr__nfet_01v8 L=0.15 W=1 nf=1 ad='int((nf+1)/2) * W/nf * 0.29' as='int((nf+2)/2) * W/nf * 0.29'
+ pd='2*int((nf+1)/2) * (W/nf + 0.29)' ps='2*int((nf+2)/2) * (W/nf + 0.29)' nrd='0.29 / W' nrs='0.29 / W'
+ sa=0 sb=0 sd=0 mult=1 m=1
XM73 GND net23 net22 GND sky130_fd_pr__nfet_01v8 L=0.15 W=1 nf=1 ad='int((nf+1)/2) * W/nf * 0.29' as='int((nf+2)/2) * W/nf * 0.29'
+ pd='2*int((nf+1)/2) * (W/nf + 0.29)' ps='2*int((nf+2)/2) * (W/nf + 0.29)' nrd='0.29 / W' nrs='0.29 / W'
+ sa=0 sb=0 sd=0 mult=1 m=1
XM74 net23 ENAD net21 GND sky130_fd_pr__nfet_01v8 L=0.15 W=1 nf=1 ad='int((nf+1)/2) * W/nf * 0.29' as='int((nf+2)/2) * W/nf * 0.29'
+ pd='2*int((nf+1)/2) * (W/nf + 0.29)' ps='2*int((nf+2)/2) * (W/nf + 0.29)' nrd='0.29 / W' nrs='0.29 / W'
+ sa=0 sb=0 sd=0 mult=1 m=1
XM75 net23 ENAD_bar net22 GND sky130_fd_pr__nfet_01v8 L=0.15 W=1 nf=1 ad='int((nf+1)/2) * W/nf * 0.29'
+ as='int((nf+2)/2) * W/nf * 0.29' pd='2*int((nf+1)/2) * (W/nf + 0.29)' ps='2*int((nf+2)/2) * (W/nf + 0.29)'
+ nrd='0.29 / W' nrs='0.29 / W' sa=0 sb=0 sd=0 mult=1 m=1
Crst net22 GND 0.1p m=1
XM76 net23 RST net22 GND sky130_fd_pr__nfet_01v8 L=0.15 W=1 nf=1 ad='int((nf+1)/2) * W/nf * 0.29' as='int((nf+2)/2) * W/nf * 0.29'
+ pd='2*int((nf+1)/2) * (W/nf + 0.29)' ps='2*int((nf+2)/2) * (W/nf + 0.29)' nrd='0.29 / W' nrs='0.29 / W'
+ sa=0 sb=0 sd=0 mult=1 m=1
Crst1 net23 GND 0.1p m=1
Vclk CLK GND pulse(0 1.8 100n 100n 100n 4.8u 10u)
Vpre PRE GND pwl(0 1.8 1u 1.8 1.1u 0)
Vrst RST GND pwl(0 1.8 1u 1.8 1.1u 0)
Venad ENAD GND 0
X15 net31 Vcp Vcn Vb bias
XM79 Aout ENAD_bar Ain VDD sky130_fd_pr__pfet_01v8 L=0.15 W=1 nf=1 ad='int((nf+1)/2) * W/nf * 0.29' as='int((nf+2)/2) * W/nf * 0.29'
+ pd='2*int((nf+1)/2) * (W/nf + 0.29)' ps='2*int((nf+2)/2) * (W/nf + 0.29)' nrd='0.29 / W' nrs='0.29 / W'
+ sa=0 sb=0 sd=0 mult=2 m=2
XM80 Aout ENAD Ain GND sky130_fd_pr__nfet_01v8 L=0.15 W=1 nf=1 ad='int((nf+1)/2) * W/nf * 0.29' as='int((nf+2)/2) * W/nf * 0.29'
+ pd='2*int((nf+1)/2) * (W/nf + 0.29)' ps='2*int((nf+2)/2) * (W/nf + 0.29)' nrd='0.29 / W' nrs='0.29 / W'
+ sa=0 sb=0 sd=0 mult=2 m=2
Vref_neg Vrefn GND 0.5
Vref_pos Vrefp GND 1.0
Vdd VDD GND 1.8
X16 STOn RCLn SH STOp RCLp SH_bar ENAD_bar PRE_bar PRE ENAD D_latch_bar D0 CLK STOp_bar STOn_bar
+ RCLp_bar RCLn_bar D1 D2 D3 RST D_latch digital_control
VD D_latch GND pwl(0 {1.8*b6} 10.2u {1.8*b6} 19.8u {1.8*b6} 20.2u {1.8*b5} 29.8u {1.8*b5} 30.1u {1.8*b4}
+ 39.8u {1.8*b4} 40.2u {1.8*b3} 49.8u {1.8*b3} 50.2u {1.8*b2} 59.8u {1.8*b2} 60.2u {1.8*b1} 69.8u {1.8*b1}
+ 70.1u {1.8*b0} 79.8u {1.8*b0})
XM77 Aout ENAD_bar COMPout_bar VDD sky130_fd_pr__pfet_01v8 L=0.15 W=1 nf=1 ad='int((nf+1)/2) * W/nf * 0.29'
+ as='int((nf+2)/2) * W/nf * 0.29' pd='2*int((nf+1)/2) * (W/nf + 0.29)' ps='2*int((nf+2)/2) * (W/nf + 0.29)'
+ nrd='0.29 / W' nrs='0.29 / W' sa=0 sb=0 sd=0 mult=2 m=2
XM78 Aout ENAD COMPout_bar GND sky130_fd_pr__nfet_01v8 L=0.15 W=1 nf=1 ad='int((nf+1)/2) * W/nf * 0.29'
+ as='int((nf+2)/2) * W/nf * 0.29' pd='2*int((nf+1)/2) * (W/nf + 0.29)' ps='2*int((nf+2)/2) * (W/nf + 0.29)'
+ nrd='0.29 / W' nrs='0.29 / W' sa=0 sb=0 sd=0 mult=2 m=2
**** begin user architecture code

.option wnflag=1
.param MC_SWITCH=0.0
.lib ~/skywater/skywater-pdk/libraries/sky130_fd_pr_ngspice/latest/models/sky130.lib.spice tt



.ic v(D_latch)=0 v(D2)=0 v(D1)=0 v(D0)=0
.ic v(D_latch_bar)=1.8 v(x16.D2_bar)=1.8 v(x16.D1_bar)=1.8 v(x16.D0_bar)=1.8
.param b6 = 0
.param b5 = 0
.param b4 = 0
.param b3 = 0
.param b2 = 0
.param b1 = 0
.param b0 = 0
.control
  set wr_vecnames
  set wr_singlescale
  let code = 0
  while code < 128
    if code eq 0
      alterparam b0 = 0
    else
      alterparam b0 = {$&code % 2}
    end
    if floor(code / 2) eq 0
      alterparam b1 = 0
    else
      alterparam b1 = {floor($&code / 2) % 2}
    end
    if floor(code / 4) eq 0
      alterparam b2 = 0
    else
      alterparam b2 = {floor($&code / 4) % 2}
    end
    if floor(code / 8) eq 0
      alterparam b3 = 0
    else
      alterparam b3 = {floor($&code / 8) % 2}
    end
    if floor(code / 16) eq 0
      alterparam b4 = 0
    else
      alterparam b4 = {floor($&code / 16) % 2}
    end
    if floor(code / 32) eq 0
      alterparam b5 = 0
    else
      alterparam b5 = {floor($&code / 32) % 2}
    end
    if floor(code / 64) eq 0
      alterparam b6 = 0
    else
      alterparam b6 = {floor($&code / 64) % 2}
    end
    reset
    save all
    tran 20n 87u
    wrdata ~/Documents/algorithmic-ada-converter/python/dac/dac_7bit.txt v(D_latch) v(Aout)
+ v(SH_neg) v(SH_pos)
    if code eq 0
      set appendwrite
      set wr_vecnames = FALSE
    end
    let code = code + 1
  end
.endc

**** end user architecture code
**.ends
.GLOBAL GND
.GLOBAL VDD
.end
